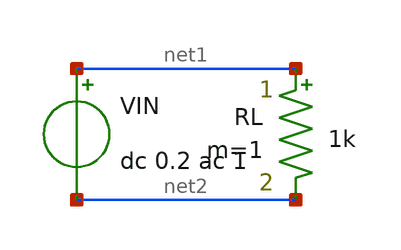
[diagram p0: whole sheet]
** sch_path: platform/packages/spicexplorer-netlist2xschem/tests/fixtures/xvport/tb_source.sch
**.subckt tb_source
VIN net1 net2 dc 0.2 ac 1
RL net1 net2 1k m=1
**.ends
.end
